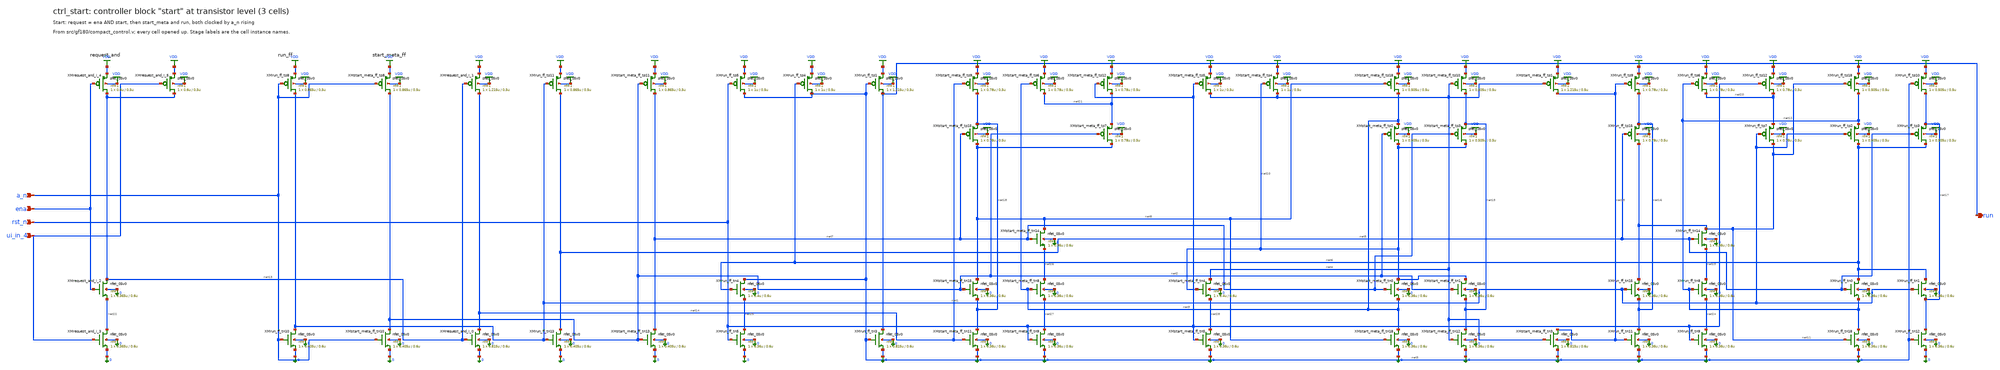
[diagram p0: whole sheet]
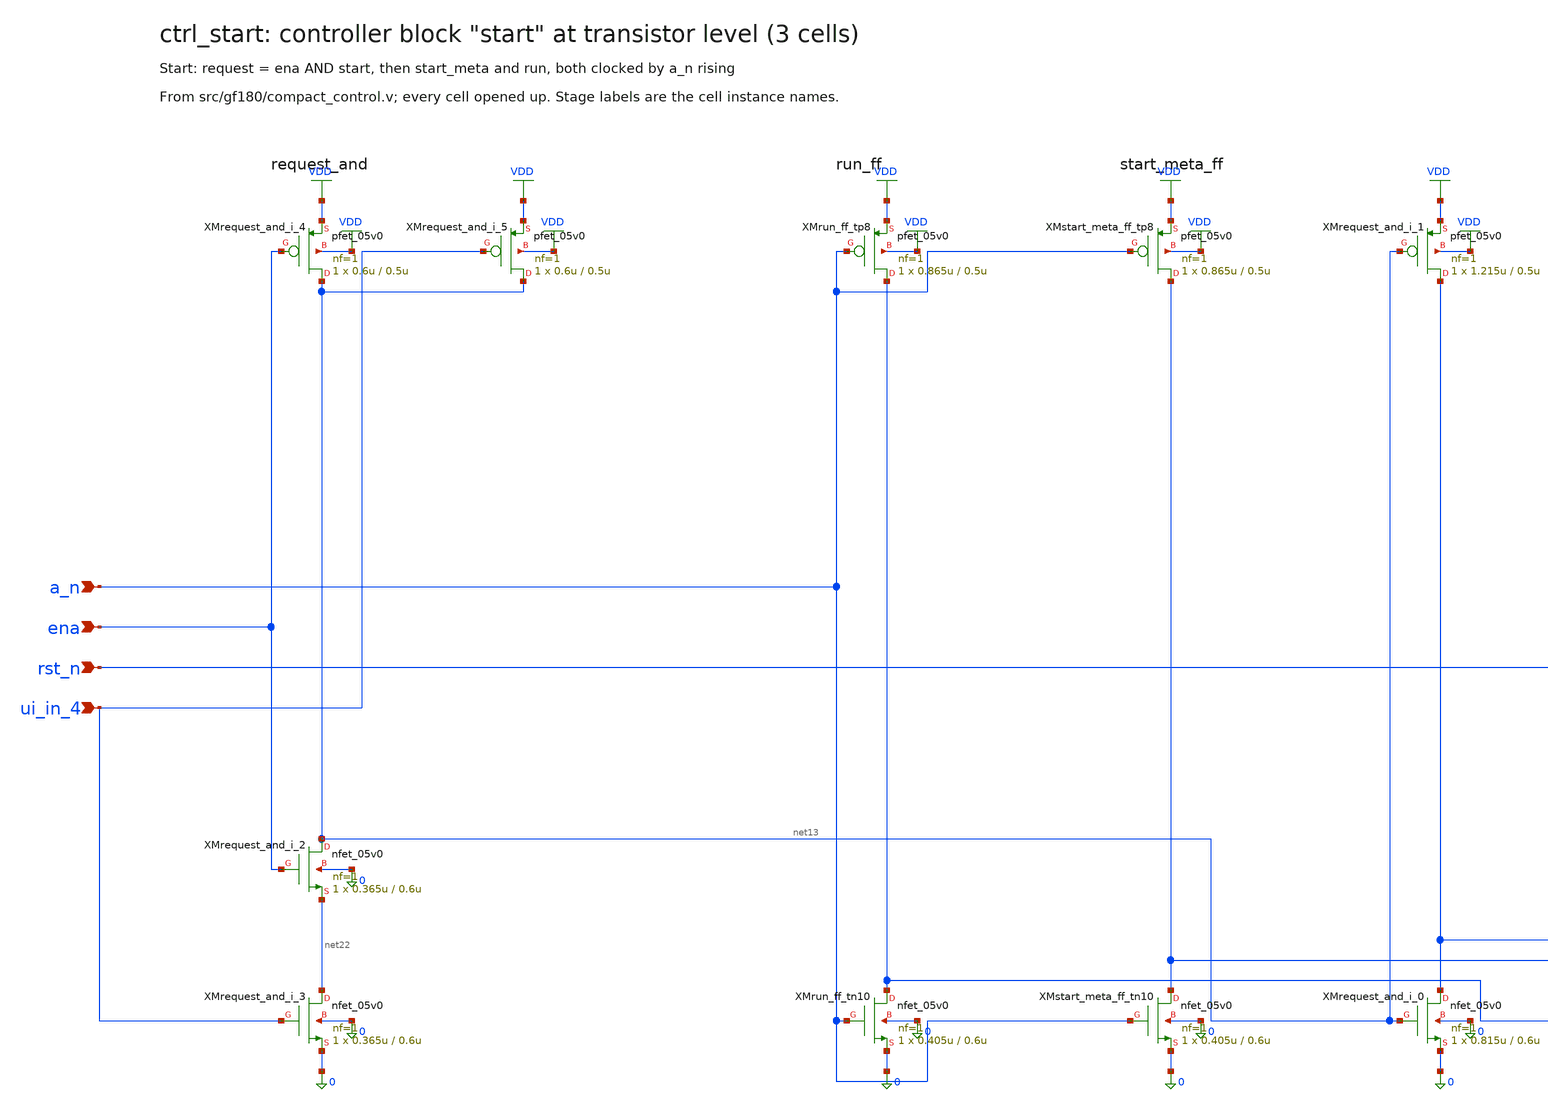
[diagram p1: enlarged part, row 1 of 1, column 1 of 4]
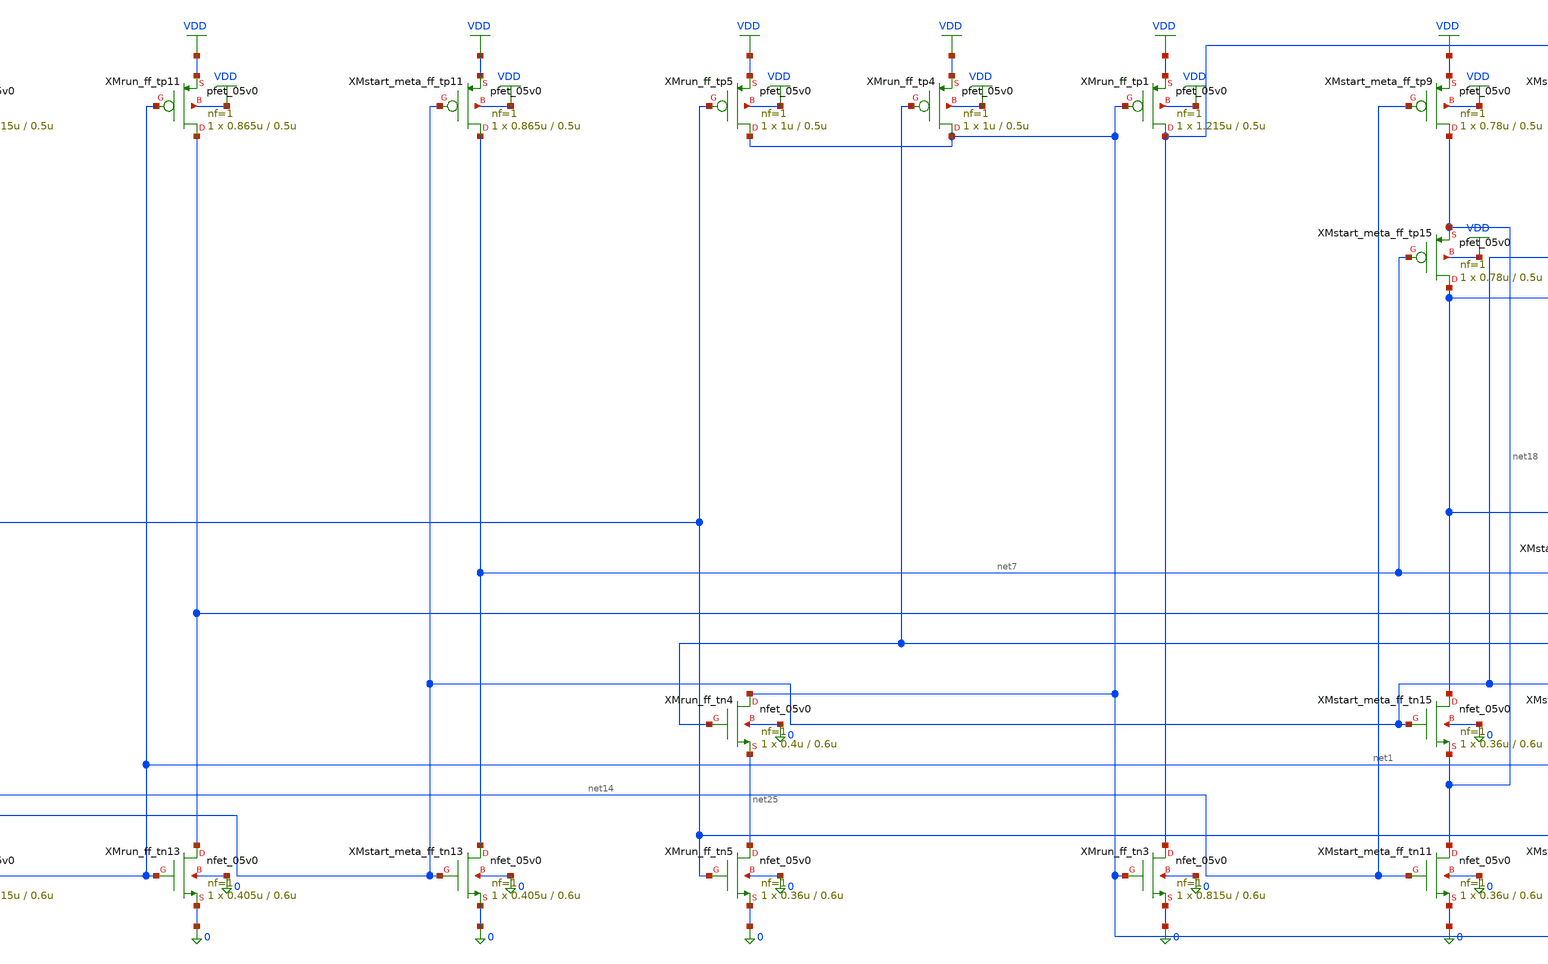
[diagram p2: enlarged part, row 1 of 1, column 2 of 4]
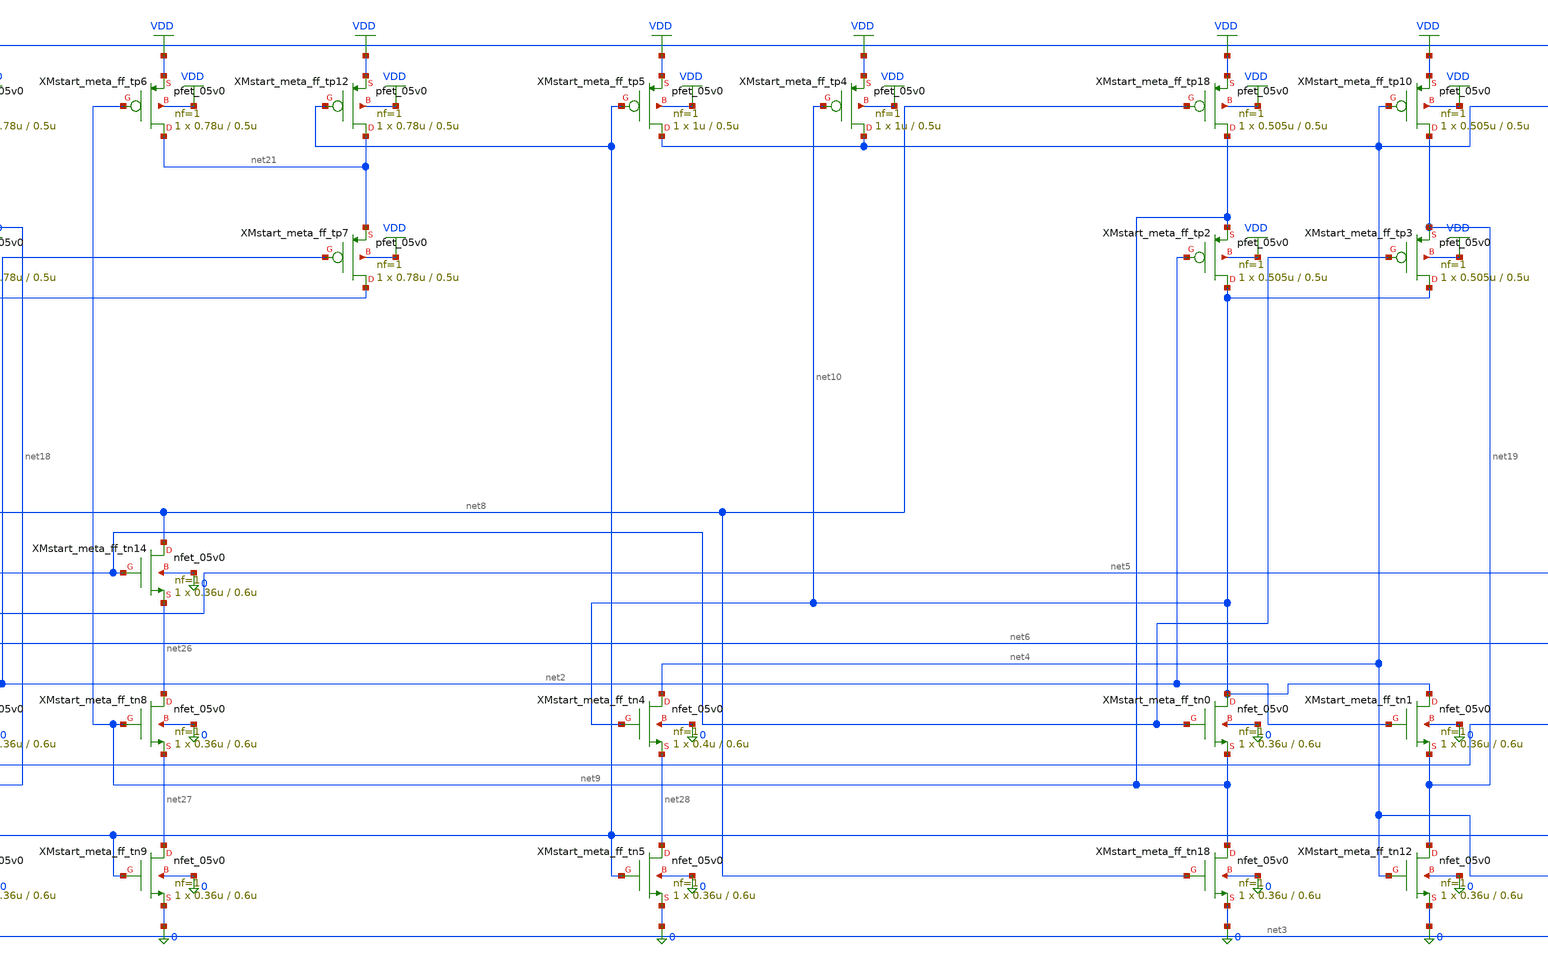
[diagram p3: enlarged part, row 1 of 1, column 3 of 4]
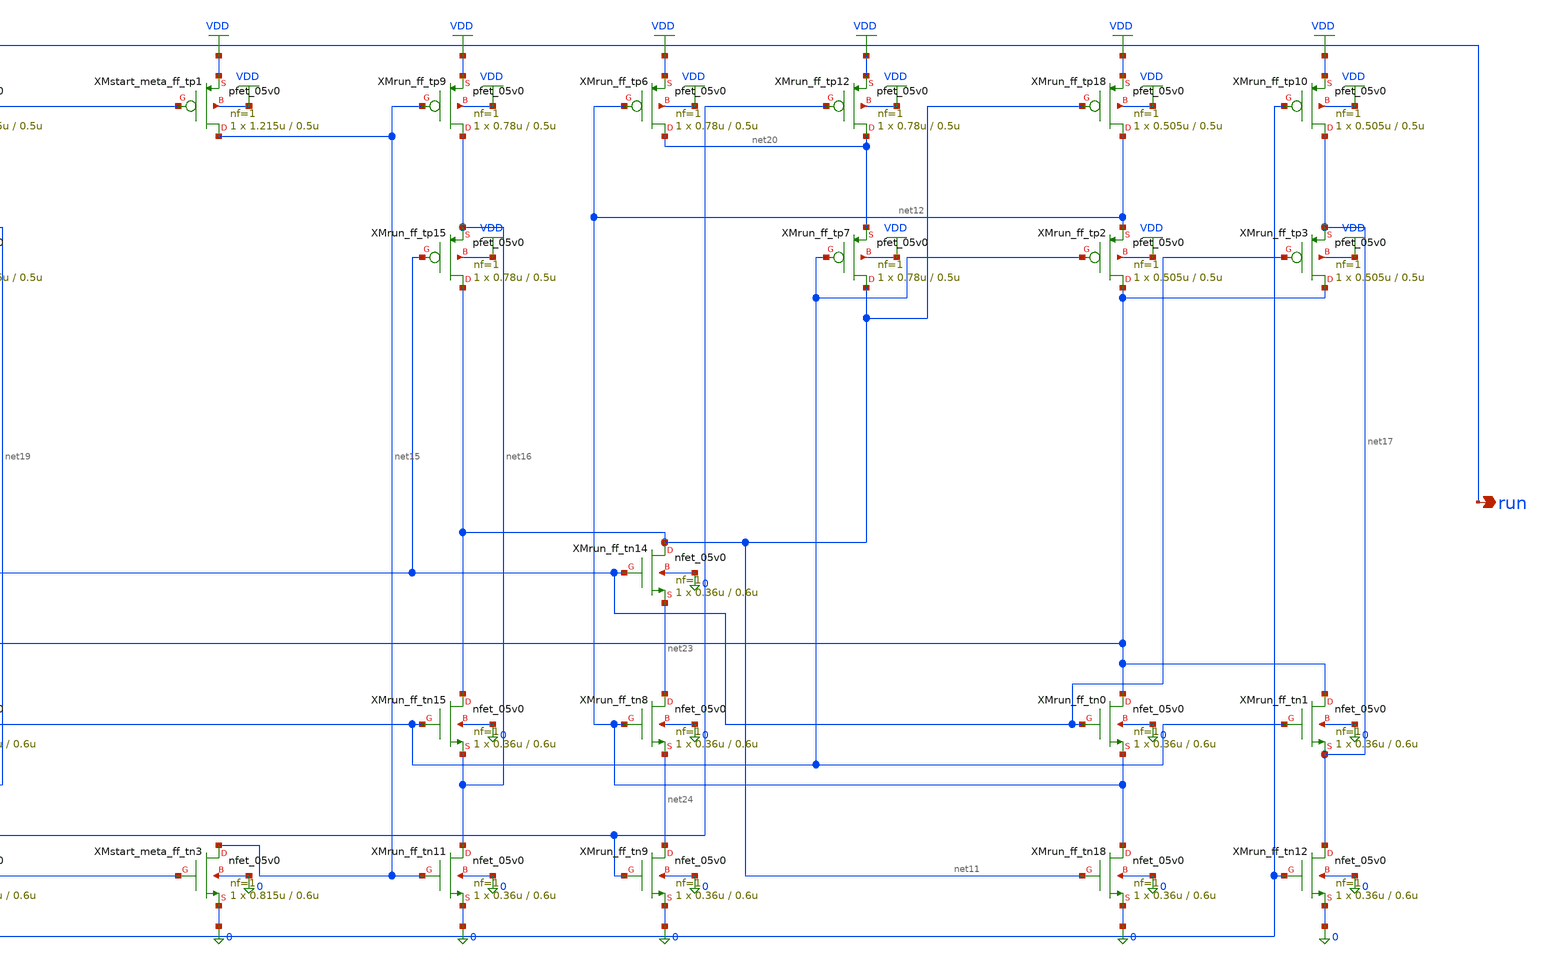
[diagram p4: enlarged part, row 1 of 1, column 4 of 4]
** sch_path: xschem/flat/ctrl_start.sch
**.subckt ctrl_start a_n ena rst_n ui_in_4 run
*.ipin a_n
*.ipin ena
*.ipin rst_n
*.ipin ui_in_4
*.opin run
XMrequest_and_i_2 net13 ena net22 0 nfet_05v0 L=0.6u W=0.365u nf=1 ad=1.825e-13 as=1.825e-13
+ pd=1.73e-06 ps=1.73e-06 nrd=0 nrs=0 sa=0 sb=0 sd=0 m=1
XMrequest_and_i_3 net22 ui_in_4 0 0 nfet_05v0 L=0.6u W=0.365u nf=1 ad=1.825e-13 as=1.825e-13
+ pd=1.73e-06 ps=1.73e-06 nrd=0 nrs=0 sa=0 sb=0 sd=0 m=1
XMrequest_and_i_0 net14 net13 0 0 nfet_05v0 L=0.6u W=0.815u nf=1 ad=4.075e-13 as=4.075e-13
+ pd=2.63e-06 ps=2.63e-06 nrd=0 nrs=0 sa=0 sb=0 sd=0 m=1
XMrequest_and_i_4 net13 ena VDD VDD pfet_05v0 L=0.5u W=0.6u nf=1 ad=3e-13 as=3e-13 pd=2.2e-06
+ ps=2.2e-06 nrd=0 nrs=0 sa=0 sb=0 sd=0 m=1
XMrequest_and_i_5 net13 ui_in_4 VDD VDD pfet_05v0 L=0.5u W=0.6u nf=1 ad=3e-13 as=3e-13 pd=2.2e-06
+ ps=2.2e-06 nrd=0 nrs=0 sa=0 sb=0 sd=0 m=1
XMrequest_and_i_1 net14 net13 VDD VDD pfet_05v0 L=0.5u W=1.215u nf=1 ad=6.075e-13 as=6.075e-13
+ pd=3.43e-06 ps=3.43e-06 nrd=0 nrs=0 sa=0 sb=0 sd=0 m=1
XMrun_ff_tn10 net1 a_n 0 0 nfet_05v0 L=0.6u W=0.405u nf=1 ad=2.025e-13 as=2.025e-13 pd=1.81e-06
+ ps=1.81e-06 nrd=0 nrs=0 sa=0 sb=0 sd=0 m=1
XMrun_ff_tn13 net5 net1 0 0 nfet_05v0 L=0.6u W=0.405u nf=1 ad=2.025e-13 as=2.025e-13 pd=1.81e-06
+ ps=1.81e-06 nrd=0 nrs=0 sa=0 sb=0 sd=0 m=1
XMrun_ff_tn11 net16 net15 0 0 nfet_05v0 L=0.6u W=0.36u nf=1 ad=1.8e-13 as=1.8e-13 pd=1.72e-06
+ ps=1.72e-06 nrd=0 nrs=0 sa=0 sb=0 sd=0 m=1
XMrun_ff_tn15 net11 net1 net16 0 nfet_05v0 L=0.6u W=0.36u nf=1 ad=1.8e-13 as=1.8e-13 pd=1.72e-06
+ ps=1.72e-06 nrd=0 nrs=0 sa=0 sb=0 sd=0 m=1
XMrun_ff_tn14 net11 net5 net23 0 nfet_05v0 L=0.6u W=0.36u nf=1 ad=1.8e-13 as=1.8e-13 pd=1.72e-06
+ ps=1.72e-06 nrd=0 nrs=0 sa=0 sb=0 sd=0 m=1
XMrun_ff_tn8 net23 net12 net24 0 nfet_05v0 L=0.6u W=0.36u nf=1 ad=1.8e-13 as=1.8e-13 pd=1.72e-06
+ ps=1.72e-06 nrd=0 nrs=0 sa=0 sb=0 sd=0 m=1
XMrun_ff_tn9 net24 rst_n 0 0 nfet_05v0 L=0.6u W=0.36u nf=1 ad=1.8e-13 as=1.8e-13 pd=1.72e-06
+ ps=1.72e-06 nrd=0 nrs=0 sa=0 sb=0 sd=0 m=1
XMrun_ff_tn18 net12 net11 0 0 nfet_05v0 L=0.6u W=0.36u nf=1 ad=1.8e-13 as=1.8e-13 pd=1.72e-06
+ ps=1.72e-06 nrd=0 nrs=0 sa=0 sb=0 sd=0 m=1
XMrun_ff_tn0 net6 net5 net12 0 nfet_05v0 L=0.6u W=0.36u nf=1 ad=1.8e-13 as=1.8e-13 pd=1.72e-06
+ ps=1.72e-06 nrd=0 nrs=0 sa=0 sb=0 sd=0 m=1
XMrun_ff_tn1 net6 net1 net17 0 nfet_05v0 L=0.6u W=0.36u nf=1 ad=1.8e-13 as=1.8e-13 pd=1.72e-06
+ ps=1.72e-06 nrd=0 nrs=0 sa=0 sb=0 sd=0 m=1
XMrun_ff_tn12 net17 net3 0 0 nfet_05v0 L=0.6u W=0.36u nf=1 ad=1.8e-13 as=1.8e-13 pd=1.72e-06
+ ps=1.72e-06 nrd=0 nrs=0 sa=0 sb=0 sd=0 m=1
XMrun_ff_tn5 net25 rst_n 0 0 nfet_05v0 L=0.6u W=0.36u nf=1 ad=1.8e-13 as=1.8e-13 pd=1.72e-06
+ ps=1.72e-06 nrd=0 nrs=0 sa=0 sb=0 sd=0 m=1
XMrun_ff_tn4 net3 net6 net25 0 nfet_05v0 L=0.6u W=0.4u nf=1 ad=2e-13 as=2e-13 pd=1.8e-06 ps=1.8e-06
+ nrd=0 nrs=0 sa=0 sb=0 sd=0 m=1
XMrun_ff_tn3 run net3 0 0 nfet_05v0 L=0.6u W=0.815u nf=1 ad=4.075e-13 as=4.075e-13 pd=2.63e-06
+ ps=2.63e-06 nrd=0 nrs=0 sa=0 sb=0 sd=0 m=1
XMrun_ff_tp8 net1 a_n VDD VDD pfet_05v0 L=0.5u W=0.865u nf=1 ad=4.325e-13 as=4.325e-13 pd=2.73e-06
+ ps=2.73e-06 nrd=0 nrs=0 sa=0 sb=0 sd=0 m=1
XMrun_ff_tp11 net5 net1 VDD VDD pfet_05v0 L=0.5u W=0.865u nf=1 ad=4.325e-13 as=4.325e-13 pd=2.73e-06
+ ps=2.73e-06 nrd=0 nrs=0 sa=0 sb=0 sd=0 m=1
XMrun_ff_tp9 net16 net15 VDD VDD pfet_05v0 L=0.5u W=0.78u nf=1 ad=3.9e-13 as=3.9e-13 pd=2.56e-06
+ ps=2.56e-06 nrd=0 nrs=0 sa=0 sb=0 sd=0 m=1
XMrun_ff_tp15 net11 net5 net16 VDD pfet_05v0 L=0.5u W=0.78u nf=1 ad=3.9e-13 as=3.9e-13 pd=2.56e-06
+ ps=2.56e-06 nrd=0 nrs=0 sa=0 sb=0 sd=0 m=1
XMrun_ff_tp7 net11 net1 net20 VDD pfet_05v0 L=0.5u W=0.78u nf=1 ad=3.9e-13 as=3.9e-13 pd=2.56e-06
+ ps=2.56e-06 nrd=0 nrs=0 sa=0 sb=0 sd=0 m=1
XMrun_ff_tp6 net20 net12 VDD VDD pfet_05v0 L=0.5u W=0.78u nf=1 ad=3.9e-13 as=3.9e-13 pd=2.56e-06
+ ps=2.56e-06 nrd=0 nrs=0 sa=0 sb=0 sd=0 m=1
XMrun_ff_tp12 net20 rst_n VDD VDD pfet_05v0 L=0.5u W=0.78u nf=1 ad=3.9e-13 as=3.9e-13 pd=2.56e-06
+ ps=2.56e-06 nrd=0 nrs=0 sa=0 sb=0 sd=0 m=1
XMrun_ff_tp18 net12 net11 VDD VDD pfet_05v0 L=0.5u W=0.505u nf=1 ad=2.525e-13 as=2.525e-13
+ pd=2.01e-06 ps=2.01e-06 nrd=0 nrs=0 sa=0 sb=0 sd=0 m=1
XMrun_ff_tp2 net6 net1 net12 VDD pfet_05v0 L=0.5u W=0.505u nf=1 ad=2.525e-13 as=2.525e-13
+ pd=2.01e-06 ps=2.01e-06 nrd=0 nrs=0 sa=0 sb=0 sd=0 m=1
XMrun_ff_tp3 net6 net5 net17 VDD pfet_05v0 L=0.5u W=0.505u nf=1 ad=2.525e-13 as=2.525e-13
+ pd=2.01e-06 ps=2.01e-06 nrd=0 nrs=0 sa=0 sb=0 sd=0 m=1
XMrun_ff_tp10 net17 net3 VDD VDD pfet_05v0 L=0.5u W=0.505u nf=1 ad=2.525e-13 as=2.525e-13
+ pd=2.01e-06 ps=2.01e-06 nrd=0 nrs=0 sa=0 sb=0 sd=0 m=1
XMrun_ff_tp5 net3 rst_n VDD VDD pfet_05v0 L=0.5u W=1u nf=1 ad=5e-13 as=5e-13 pd=3e-06 ps=3e-06 nrd=0
+ nrs=0 sa=0 sb=0 sd=0 m=1
XMrun_ff_tp4 net3 net6 VDD VDD pfet_05v0 L=0.5u W=1u nf=1 ad=5e-13 as=5e-13 pd=3e-06 ps=3e-06 nrd=0
+ nrs=0 sa=0 sb=0 sd=0 m=1
XMrun_ff_tp1 run net3 VDD VDD pfet_05v0 L=0.5u W=1.215u nf=1 ad=6.075e-13 as=6.075e-13 pd=3.43e-06
+ ps=3.43e-06 nrd=0 nrs=0 sa=0 sb=0 sd=0 m=1
XMstart_meta_ff_tn10 net2 a_n 0 0 nfet_05v0 L=0.6u W=0.405u nf=1 ad=2.025e-13 as=2.025e-13
+ pd=1.81e-06 ps=1.81e-06 nrd=0 nrs=0 sa=0 sb=0 sd=0 m=1
XMstart_meta_ff_tn13 net7 net2 0 0 nfet_05v0 L=0.6u W=0.405u nf=1 ad=2.025e-13 as=2.025e-13
+ pd=1.81e-06 ps=1.81e-06 nrd=0 nrs=0 sa=0 sb=0 sd=0 m=1
XMstart_meta_ff_tn11 net18 net14 0 0 nfet_05v0 L=0.6u W=0.36u nf=1 ad=1.8e-13 as=1.8e-13 pd=1.72e-06
+ ps=1.72e-06 nrd=0 nrs=0 sa=0 sb=0 sd=0 m=1
XMstart_meta_ff_tn15 net8 net2 net18 0 nfet_05v0 L=0.6u W=0.36u nf=1 ad=1.8e-13 as=1.8e-13
+ pd=1.72e-06 ps=1.72e-06 nrd=0 nrs=0 sa=0 sb=0 sd=0 m=1
XMstart_meta_ff_tn14 net8 net7 net26 0 nfet_05v0 L=0.6u W=0.36u nf=1 ad=1.8e-13 as=1.8e-13
+ pd=1.72e-06 ps=1.72e-06 nrd=0 nrs=0 sa=0 sb=0 sd=0 m=1
XMstart_meta_ff_tn8 net26 net9 net27 0 nfet_05v0 L=0.6u W=0.36u nf=1 ad=1.8e-13 as=1.8e-13
+ pd=1.72e-06 ps=1.72e-06 nrd=0 nrs=0 sa=0 sb=0 sd=0 m=1
XMstart_meta_ff_tn9 net27 rst_n 0 0 nfet_05v0 L=0.6u W=0.36u nf=1 ad=1.8e-13 as=1.8e-13 pd=1.72e-06
+ ps=1.72e-06 nrd=0 nrs=0 sa=0 sb=0 sd=0 m=1
XMstart_meta_ff_tn18 net9 net8 0 0 nfet_05v0 L=0.6u W=0.36u nf=1 ad=1.8e-13 as=1.8e-13 pd=1.72e-06
+ ps=1.72e-06 nrd=0 nrs=0 sa=0 sb=0 sd=0 m=1
XMstart_meta_ff_tn0 net10 net7 net9 0 nfet_05v0 L=0.6u W=0.36u nf=1 ad=1.8e-13 as=1.8e-13
+ pd=1.72e-06 ps=1.72e-06 nrd=0 nrs=0 sa=0 sb=0 sd=0 m=1
XMstart_meta_ff_tn1 net10 net2 net19 0 nfet_05v0 L=0.6u W=0.36u nf=1 ad=1.8e-13 as=1.8e-13
+ pd=1.72e-06 ps=1.72e-06 nrd=0 nrs=0 sa=0 sb=0 sd=0 m=1
XMstart_meta_ff_tn12 net19 net4 0 0 nfet_05v0 L=0.6u W=0.36u nf=1 ad=1.8e-13 as=1.8e-13 pd=1.72e-06
+ ps=1.72e-06 nrd=0 nrs=0 sa=0 sb=0 sd=0 m=1
XMstart_meta_ff_tn5 net28 rst_n 0 0 nfet_05v0 L=0.6u W=0.36u nf=1 ad=1.8e-13 as=1.8e-13 pd=1.72e-06
+ ps=1.72e-06 nrd=0 nrs=0 sa=0 sb=0 sd=0 m=1
XMstart_meta_ff_tn4 net4 net10 net28 0 nfet_05v0 L=0.6u W=0.4u nf=1 ad=2e-13 as=2e-13 pd=1.8e-06
+ ps=1.8e-06 nrd=0 nrs=0 sa=0 sb=0 sd=0 m=1
XMstart_meta_ff_tn3 net15 net4 0 0 nfet_05v0 L=0.6u W=0.815u nf=1 ad=4.075e-13 as=4.075e-13
+ pd=2.63e-06 ps=2.63e-06 nrd=0 nrs=0 sa=0 sb=0 sd=0 m=1
XMstart_meta_ff_tp8 net2 a_n VDD VDD pfet_05v0 L=0.5u W=0.865u nf=1 ad=4.325e-13 as=4.325e-13
+ pd=2.73e-06 ps=2.73e-06 nrd=0 nrs=0 sa=0 sb=0 sd=0 m=1
XMstart_meta_ff_tp11 net7 net2 VDD VDD pfet_05v0 L=0.5u W=0.865u nf=1 ad=4.325e-13 as=4.325e-13
+ pd=2.73e-06 ps=2.73e-06 nrd=0 nrs=0 sa=0 sb=0 sd=0 m=1
XMstart_meta_ff_tp9 net18 net14 VDD VDD pfet_05v0 L=0.5u W=0.78u nf=1 ad=3.9e-13 as=3.9e-13
+ pd=2.56e-06 ps=2.56e-06 nrd=0 nrs=0 sa=0 sb=0 sd=0 m=1
XMstart_meta_ff_tp15 net8 net7 net18 VDD pfet_05v0 L=0.5u W=0.78u nf=1 ad=3.9e-13 as=3.9e-13
+ pd=2.56e-06 ps=2.56e-06 nrd=0 nrs=0 sa=0 sb=0 sd=0 m=1
XMstart_meta_ff_tp7 net8 net2 net21 VDD pfet_05v0 L=0.5u W=0.78u nf=1 ad=3.9e-13 as=3.9e-13
+ pd=2.56e-06 ps=2.56e-06 nrd=0 nrs=0 sa=0 sb=0 sd=0 m=1
XMstart_meta_ff_tp6 net21 net9 VDD VDD pfet_05v0 L=0.5u W=0.78u nf=1 ad=3.9e-13 as=3.9e-13
+ pd=2.56e-06 ps=2.56e-06 nrd=0 nrs=0 sa=0 sb=0 sd=0 m=1
XMstart_meta_ff_tp12 net21 rst_n VDD VDD pfet_05v0 L=0.5u W=0.78u nf=1 ad=3.9e-13 as=3.9e-13
+ pd=2.56e-06 ps=2.56e-06 nrd=0 nrs=0 sa=0 sb=0 sd=0 m=1
XMstart_meta_ff_tp18 net9 net8 VDD VDD pfet_05v0 L=0.5u W=0.505u nf=1 ad=2.525e-13 as=2.525e-13
+ pd=2.01e-06 ps=2.01e-06 nrd=0 nrs=0 sa=0 sb=0 sd=0 m=1
XMstart_meta_ff_tp2 net10 net2 net9 VDD pfet_05v0 L=0.5u W=0.505u nf=1 ad=2.525e-13 as=2.525e-13
+ pd=2.01e-06 ps=2.01e-06 nrd=0 nrs=0 sa=0 sb=0 sd=0 m=1
XMstart_meta_ff_tp3 net10 net7 net19 VDD pfet_05v0 L=0.5u W=0.505u nf=1 ad=2.525e-13 as=2.525e-13
+ pd=2.01e-06 ps=2.01e-06 nrd=0 nrs=0 sa=0 sb=0 sd=0 m=1
XMstart_meta_ff_tp10 net19 net4 VDD VDD pfet_05v0 L=0.5u W=0.505u nf=1 ad=2.525e-13 as=2.525e-13
+ pd=2.01e-06 ps=2.01e-06 nrd=0 nrs=0 sa=0 sb=0 sd=0 m=1
XMstart_meta_ff_tp5 net4 rst_n VDD VDD pfet_05v0 L=0.5u W=1u nf=1 ad=5e-13 as=5e-13 pd=3e-06
+ ps=3e-06 nrd=0 nrs=0 sa=0 sb=0 sd=0 m=1
XMstart_meta_ff_tp4 net4 net10 VDD VDD pfet_05v0 L=0.5u W=1u nf=1 ad=5e-13 as=5e-13 pd=3e-06
+ ps=3e-06 nrd=0 nrs=0 sa=0 sb=0 sd=0 m=1
XMstart_meta_ff_tp1 net15 net4 VDD VDD pfet_05v0 L=0.5u W=1.215u nf=1 ad=6.075e-13 as=6.075e-13
+ pd=3.43e-06 ps=3.43e-06 nrd=0 nrs=0 sa=0 sb=0 sd=0 m=1
**.ends
.GLOBAL VDD
.end
